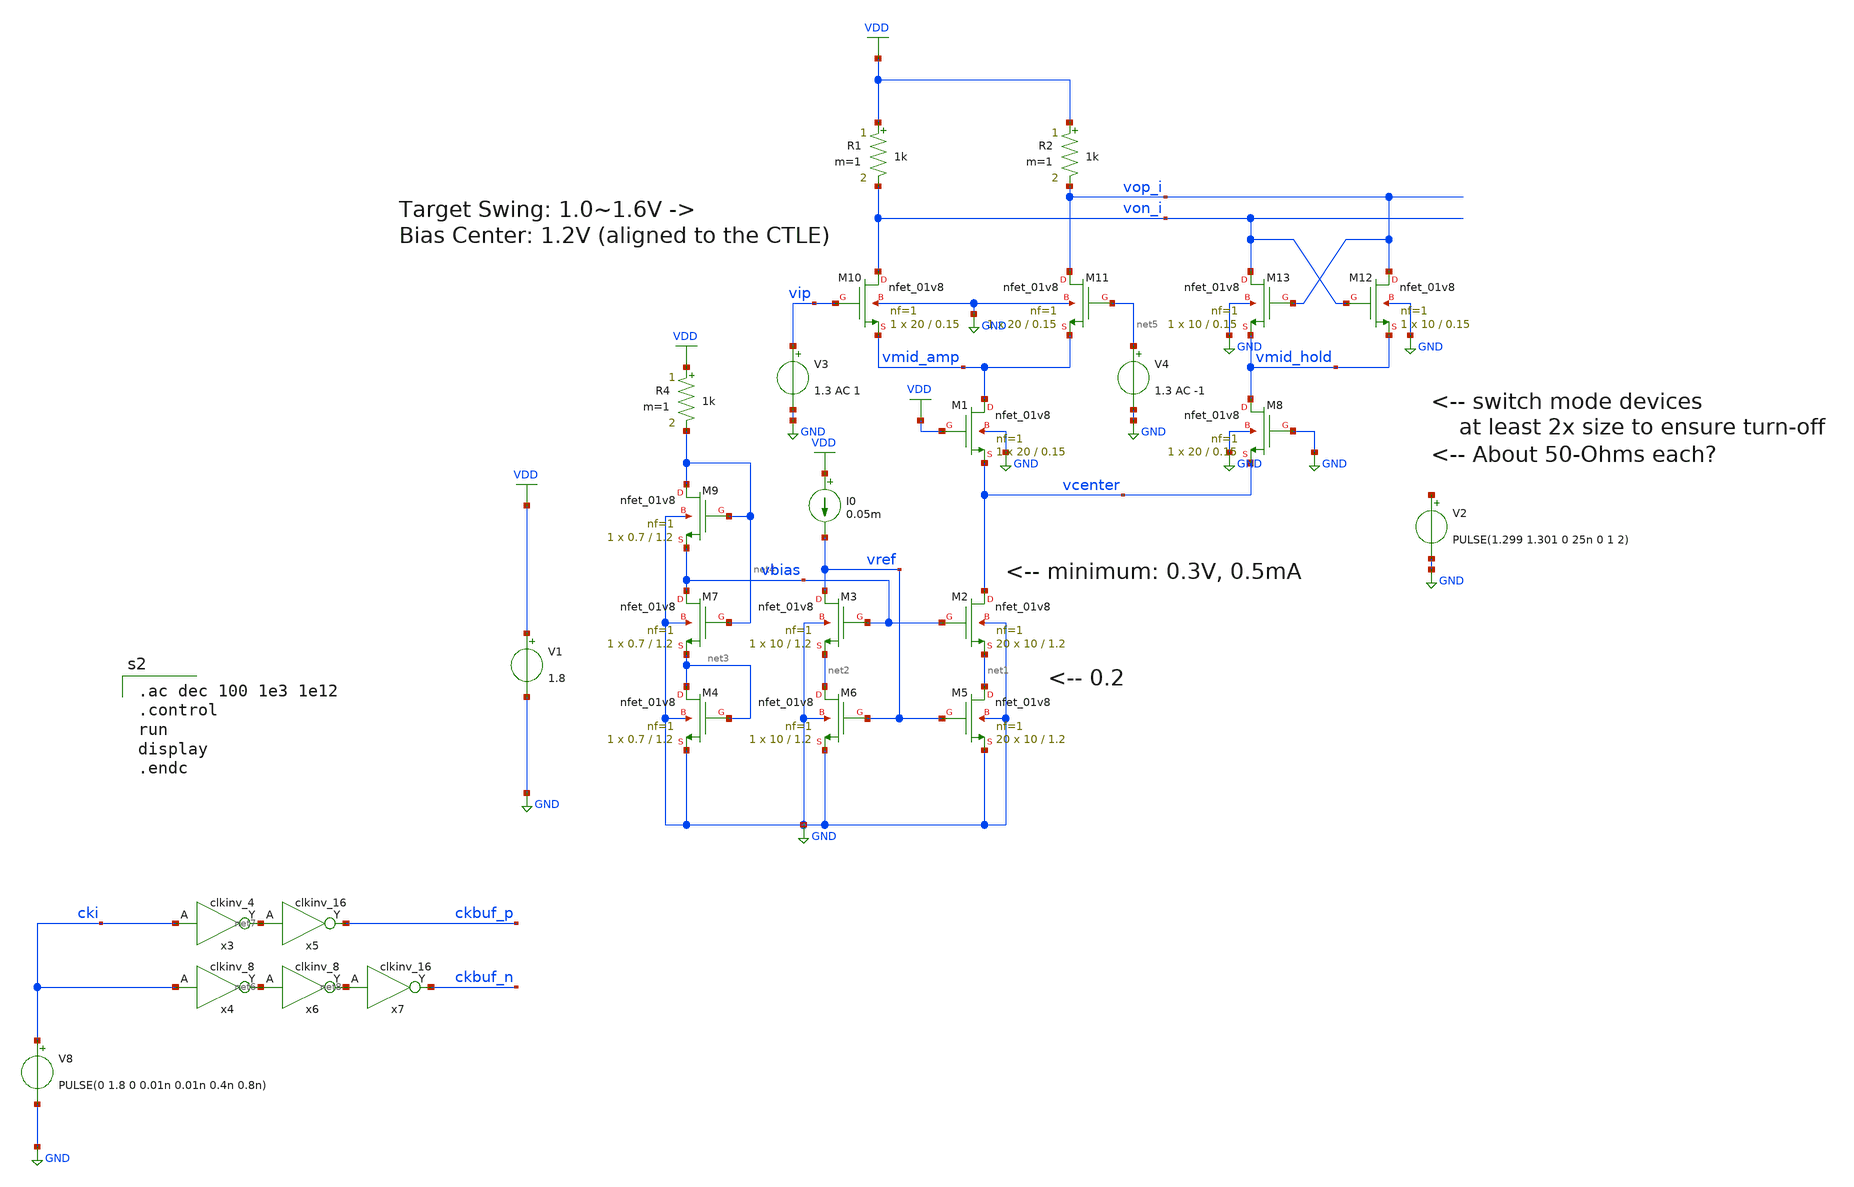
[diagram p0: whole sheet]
** sch_path: xschem/CML_latch_1mA_tb.sch
**.subckt CML_latch_1mA_tb
V1 VDD GND 1.8
XM5 net1 vref GND GND sky130_fd_pr__nfet_01v8 L=1.2 W=10 nf=1 ad='int((nf+1)/2) * W/nf * 0.29' as='int((nf+2)/2) * W/nf * 0.29'
+ pd='2*int((nf+1)/2) * (W/nf + 0.29)' ps='2*int((nf+2)/2) * (W/nf + 0.29)' nrd='0.29 / W' nrs='0.29 / W'
+ sa=0 sb=0 sd=0 mult=20 m=20
XM6 net2 vref GND GND sky130_fd_pr__nfet_01v8 L=1.2 W=10 nf=1 ad='int((nf+1)/2) * W/nf * 0.29' as='int((nf+2)/2) * W/nf * 0.29'
+ pd='2*int((nf+1)/2) * (W/nf + 0.29)' ps='2*int((nf+2)/2) * (W/nf + 0.29)' nrd='0.29 / W' nrs='0.29 / W'
+ sa=0 sb=0 sd=0 mult=1 m=1
I0 VDD vref 0.05m
XM2 vcenter vbias net1 GND sky130_fd_pr__nfet_01v8 L=1.2 W=10 nf=1 ad='int((nf+1)/2) * W/nf * 0.29' as='int((nf+2)/2) * W/nf * 0.29'
+ pd='2*int((nf+1)/2) * (W/nf + 0.29)' ps='2*int((nf+2)/2) * (W/nf + 0.29)' nrd='0.29 / W' nrs='0.29 / W'
+ sa=0 sb=0 sd=0 mult=20 m=20
XM3 vref vbias net2 GND sky130_fd_pr__nfet_01v8 L=1.2 W=10 nf=1 ad='int((nf+1)/2) * W/nf * 0.29' as='int((nf+2)/2) * W/nf * 0.29'
+ pd='2*int((nf+1)/2) * (W/nf + 0.29)' ps='2*int((nf+2)/2) * (W/nf + 0.29)' nrd='0.29 / W' nrs='0.29 / W'
+ sa=0 sb=0 sd=0 mult=1 m=1
XM4 net3 net3 GND GND sky130_fd_pr__nfet_01v8 L=1.2 W=0.7 nf=1 ad='int((nf+1)/2) * W/nf * 0.29' as='int((nf+2)/2) * W/nf * 0.29'
+ pd='2*int((nf+1)/2) * (W/nf + 0.29)' ps='2*int((nf+2)/2) * (W/nf + 0.29)' nrd='0.29 / W' nrs='0.29 / W'
+ sa=0 sb=0 sd=0 mult=1 m=1
XM7 vbias net4 net3 GND sky130_fd_pr__nfet_01v8 L=1.2 W=0.7 nf=1 ad='int((nf+1)/2) * W/nf * 0.29' as='int((nf+2)/2) * W/nf * 0.29'
+ pd='2*int((nf+1)/2) * (W/nf + 0.29)' ps='2*int((nf+2)/2) * (W/nf + 0.29)' nrd='0.29 / W' nrs='0.29 / W'
+ sa=0 sb=0 sd=0 mult=1 m=1
XM9 net4 net4 vbias GND sky130_fd_pr__nfet_01v8 L=1.2 W=0.7 nf=1 ad='int((nf+1)/2) * W/nf * 0.29' as='int((nf+2)/2) * W/nf * 0.29'
+ pd='2*int((nf+1)/2) * (W/nf + 0.29)' ps='2*int((nf+2)/2) * (W/nf + 0.29)' nrd='0.29 / W' nrs='0.29 / W'
+ sa=0 sb=0 sd=0 mult=1 m=1
R4 VDD net4 1k m=1
XM1 vmid_amp VDD vcenter GND sky130_fd_pr__nfet_01v8 L=0.15 W=20 nf=1 ad='int((nf+1)/2) * W/nf * 0.29'
+ as='int((nf+2)/2) * W/nf * 0.29' pd='2*int((nf+1)/2) * (W/nf + 0.29)' ps='2*int((nf+2)/2) * (W/nf + 0.29)'
+ nrd='0.29 / W' nrs='0.29 / W' sa=0 sb=0 sd=0 mult=1 m=1
XM8 vmid_hold GND vcenter GND sky130_fd_pr__nfet_01v8 L=0.15 W=20 nf=1 ad='int((nf+1)/2) * W/nf * 0.29'
+ as='int((nf+2)/2) * W/nf * 0.29' pd='2*int((nf+1)/2) * (W/nf + 0.29)' ps='2*int((nf+2)/2) * (W/nf + 0.29)'
+ nrd='0.29 / W' nrs='0.29 / W' sa=0 sb=0 sd=0 mult=1 m=1
XM10 von_i vip vmid_amp GND sky130_fd_pr__nfet_01v8 L=0.15 W=20 nf=1 ad='int((nf+1)/2) * W/nf * 0.29'
+ as='int((nf+2)/2) * W/nf * 0.29' pd='2*int((nf+1)/2) * (W/nf + 0.29)' ps='2*int((nf+2)/2) * (W/nf + 0.29)'
+ nrd='0.29 / W' nrs='0.29 / W' sa=0 sb=0 sd=0 mult=1 m=1
XM11 vop_i net5 vmid_amp GND sky130_fd_pr__nfet_01v8 L=0.15 W=20 nf=1 ad='int((nf+1)/2) * W/nf * 0.29'
+ as='int((nf+2)/2) * W/nf * 0.29' pd='2*int((nf+1)/2) * (W/nf + 0.29)' ps='2*int((nf+2)/2) * (W/nf + 0.29)'
+ nrd='0.29 / W' nrs='0.29 / W' sa=0 sb=0 sd=0 mult=1 m=1
XM12 vop_i von_i vmid_hold GND sky130_fd_pr__nfet_01v8 L=0.15 W=10 nf=1 ad='int((nf+1)/2) * W/nf * 0.29'
+ as='int((nf+2)/2) * W/nf * 0.29' pd='2*int((nf+1)/2) * (W/nf + 0.29)' ps='2*int((nf+2)/2) * (W/nf + 0.29)'
+ nrd='0.29 / W' nrs='0.29 / W' sa=0 sb=0 sd=0 mult=1 m=1
XM13 von_i vop_i vmid_hold GND sky130_fd_pr__nfet_01v8 L=0.15 W=10 nf=1 ad='int((nf+1)/2) * W/nf * 0.29'
+ as='int((nf+2)/2) * W/nf * 0.29' pd='2*int((nf+1)/2) * (W/nf + 0.29)' ps='2*int((nf+2)/2) * (W/nf + 0.29)'
+ nrd='0.29 / W' nrs='0.29 / W' sa=0 sb=0 sd=0 mult=1 m=1
R1 VDD von_i 1k m=1
R2 VDD vop_i 1k m=1
V8 cki GND PULSE(0 1.8 0 0.01n 0.01n 0.4n 0.8n)
x4 cki gnd gnd vdd vdd net6 sky130_fd_sc_hs__clkinv_8
x3 cki gnd gnd vdd vdd net7 sky130_fd_sc_hs__clkinv_4
x5 net7 gnd gnd vdd vdd ckbuf_p sky130_fd_sc_hs__clkinv_16
x6 net6 gnd gnd vdd vdd net8 sky130_fd_sc_hs__clkinv_8
x7 net8 gnd gnd vdd vdd ckbuf_n sky130_fd_sc_hs__clkinv_16
V3 vip GND 1.3 AC 1
V2 net9 GND PULSE(1.299 1.301 0 25n 0 1 2)
V4 net5 GND 1.3 AC -1
**** begin user architecture code
.lib $::SKYWATER_MODELS/sky130.lib.spice tt
.include $::PDKPATH/libs.ref/sky130_fd_sc_hs/spice/sky130_fd_sc_hs.spice


.ac dec 100 1e3 1e12
.control
run
display
.endc


**** end user architecture code
**.ends
.GLOBAL GND
.GLOBAL VDD
.end
